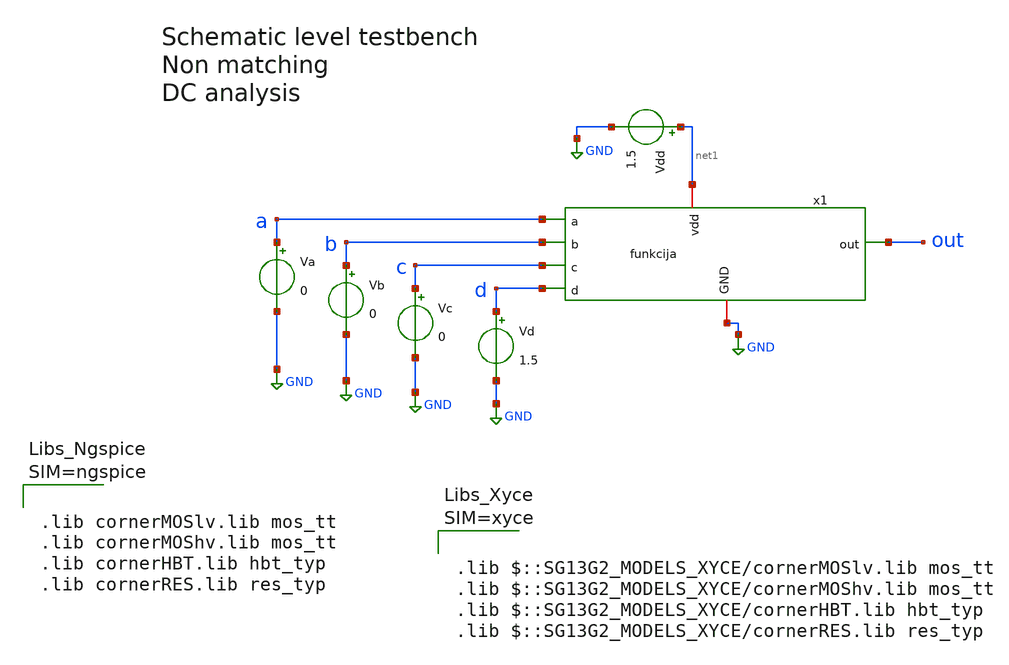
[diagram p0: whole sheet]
** sch_path: projekat/slucaj_2/testbench/tb_dc.sch
**.subckt tb_dc
Va a GND 0
Vb b GND 0
Vc c GND 0
Vd d GND 1.5
Vdd net1 GND 1.5
x1 net1 out d a c b GND funkcija
**** begin user architecture code



.lib cornerMOSlv.lib mos_tt
.lib cornerMOShv.lib mos_tt
.lib cornerHBT.lib hbt_typ
.lib cornerRES.lib res_typ









.dc Va 0 1.5 0.001

.control
  save all
  run

  * Crtanje VTC krive
  plot v(out) vs v(a)

  * Crtanje izvoda VTC krive za pronalazenje margina suma (trazi se gde je y = -1)
  *plot deriv(v(out)) vs v(a)

   wrdata /home/Nikola.Jankovic/projekat/slucaj_2/python/vtc_kriva.txt v(out)
.endc

**** end user architecture code
**.ends

* expanding   symbol:  /home/Nikola.Jankovic/projekat/slucaj_2/schematic/funkcija.sym # of pins=7
** sym_path: projekat/slucaj_2/schematic/funkcija.sym
** sch_path: projekat/slucaj_2/schematic/funkcija.sch
.subckt funkcija vdd out d a c b GND
*.ipin a
*.ipin b
*.ipin c
*.ipin d
*.iopin vdd
*.iopin GND
*.opin out
XM1 net1 a GND GND sg13_lv_nmos w=0.3u l=0.13u ng=1 m=1 mm_ok=1
XM2 net1 b GND GND sg13_lv_nmos w=0.3u l=0.13u ng=1 m=1 mm_ok=1
XM3 net1 c GND GND sg13_lv_nmos w=0.3u l=0.13u ng=1 m=1 mm_ok=1
XM4 out d net1 GND sg13_lv_nmos w=0.3u l=0.13u ng=1 m=1 mm_ok=1
XM5 net2 a vdd vdd sg13_lv_pmos w=0.9u l=0.13u ng=1 m=1 mm_ok=1
XM6 net3 b net2 vdd sg13_lv_pmos w=0.9u l=0.13u ng=1 m=1 mm_ok=1
XM7 out c net3 vdd sg13_lv_pmos w=0.9u l=0.13u ng=1 m=1 mm_ok=1
XM8 out d vdd vdd sg13_lv_pmos w=0.3u l=0.13u ng=1 m=1 mm_ok=1
.ends

.GLOBAL GND
.end
